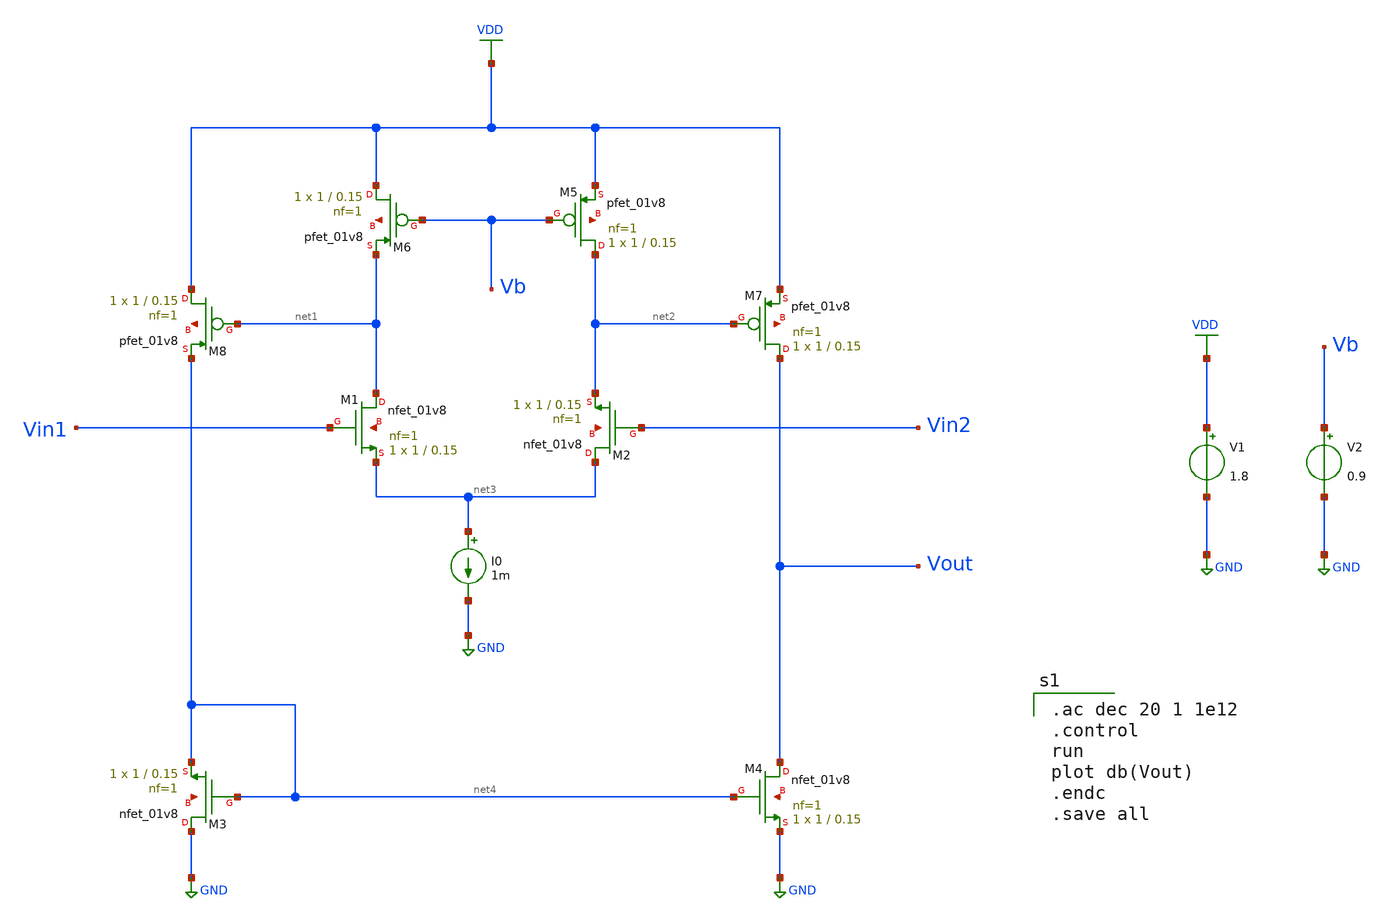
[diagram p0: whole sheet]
** sch_path: Circuits/Examples/Analog/untitled-2.sch
**.subckt untitled-2
XM1 net1 Vin1 net3 net5 sky130_fd_pr__nfet_01v8 L=0.15 W=1 nf=1 ad='int((nf+1)/2) * W/nf * 0.29' as='int((nf+2)/2) * W/nf * 0.29'
+ pd='2*int((nf+1)/2) * (W/nf + 0.29)' ps='2*int((nf+2)/2) * (W/nf + 0.29)' nrd='0.29 / W' nrs='0.29 / W'
+ sa=0 sb=0 sd=0 mult=1 m=1
XM2 net3 Vin2 net2 net6 sky130_fd_pr__nfet_01v8 L=0.15 W=1 nf=1 ad='int((nf+1)/2) * W/nf * 0.29' as='int((nf+2)/2) * W/nf * 0.29'
+ pd='2*int((nf+1)/2) * (W/nf + 0.29)' ps='2*int((nf+2)/2) * (W/nf + 0.29)' nrd='0.29 / W' nrs='0.29 / W'
+ sa=0 sb=0 sd=0 mult=1 m=1
XM3 GND net4 net4 net7 sky130_fd_pr__nfet_01v8 L=0.15 W=1 nf=1 ad='int((nf+1)/2) * W/nf * 0.29' as='int((nf+2)/2) * W/nf * 0.29'
+ pd='2*int((nf+1)/2) * (W/nf + 0.29)' ps='2*int((nf+2)/2) * (W/nf + 0.29)' nrd='0.29 / W' nrs='0.29 / W'
+ sa=0 sb=0 sd=0 mult=1 m=1
XM4 Vout net4 GND net8 sky130_fd_pr__nfet_01v8 L=0.15 W=1 nf=1 ad='int((nf+1)/2) * W/nf * 0.29' as='int((nf+2)/2) * W/nf * 0.29'
+ pd='2*int((nf+1)/2) * (W/nf + 0.29)' ps='2*int((nf+2)/2) * (W/nf + 0.29)' nrd='0.29 / W' nrs='0.29 / W'
+ sa=0 sb=0 sd=0 mult=1 m=1
XM5 net2 Vb VDD net9 sky130_fd_pr__pfet_01v8 L=0.15 W=1 nf=1 ad='int((nf+1)/2) * W/nf * 0.29' as='int((nf+2)/2) * W/nf * 0.29'
+ pd='2*int((nf+1)/2) * (W/nf + 0.29)' ps='2*int((nf+2)/2) * (W/nf + 0.29)' nrd='0.29 / W' nrs='0.29 / W'
+ sa=0 sb=0 sd=0 mult=1 m=1
XM6 VDD Vb net1 net10 sky130_fd_pr__pfet_01v8 L=0.15 W=1 nf=1 ad='int((nf+1)/2) * W/nf * 0.29' as='int((nf+2)/2) * W/nf * 0.29'
+ pd='2*int((nf+1)/2) * (W/nf + 0.29)' ps='2*int((nf+2)/2) * (W/nf + 0.29)' nrd='0.29 / W' nrs='0.29 / W'
+ sa=0 sb=0 sd=0 mult=1 m=1
XM7 Vout net2 VDD net11 sky130_fd_pr__pfet_01v8 L=0.15 W=1 nf=1 ad='int((nf+1)/2) * W/nf * 0.29' as='int((nf+2)/2) * W/nf * 0.29'
+ pd='2*int((nf+1)/2) * (W/nf + 0.29)' ps='2*int((nf+2)/2) * (W/nf + 0.29)' nrd='0.29 / W' nrs='0.29 / W'
+ sa=0 sb=0 sd=0 mult=1 m=1
XM8 VDD net1 net4 net12 sky130_fd_pr__pfet_01v8 L=0.15 W=1 nf=1 ad='int((nf+1)/2) * W/nf * 0.29' as='int((nf+2)/2) * W/nf * 0.29'
+ pd='2*int((nf+1)/2) * (W/nf + 0.29)' ps='2*int((nf+2)/2) * (W/nf + 0.29)' nrd='0.29 / W' nrs='0.29 / W'
+ sa=0 sb=0 sd=0 mult=1 m=1
I0 net3 GND 1m
V1 VDD GND 1.8
V2 Vb GND 0.9
**** begin user architecture code
 ** manual skywater pdks install (with patches applied)
* .lib $::SKYWATER_MODELS/models/sky130.lib.spice tt

** opencircuitdesign pdks install
.lib $::SKYWATER_MODELS/sky130.lib.spice tt

.param mc_mm_switch=0
.param mc_pr_switch=0


.ac dec 20 1 1e12
.control
run
plot db(Vout)
.endc
.save all

**** end user architecture code
**.ends
.GLOBAL GND
.GLOBAL VDD
.end
